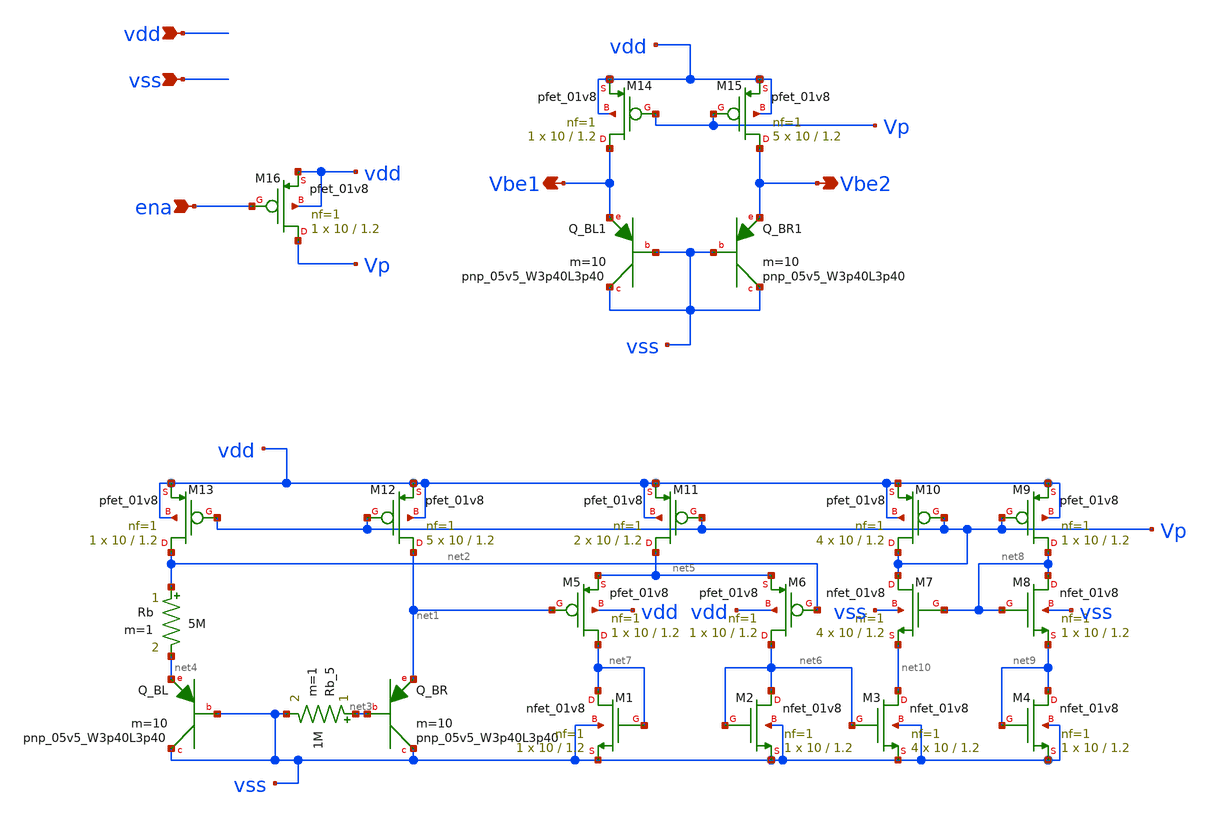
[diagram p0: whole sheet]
** sch_path: xschem/sky130_od_ip__tempsensor.sch
**.subckt sky130_od_ip__tempsensor vdd vss Vbe2 Vbe1 ena
*.ipin vdd
*.ipin vss
*.opin Vbe2
*.opin Vbe1
*.ipin ena
XM12 net1 Vp vdd vdd sky130_fd_pr__pfet_01v8 L=1.2 W=10 nf=1 ad='int((nf+1)/2) * W/nf * 0.29' as='int((nf+2)/2) * W/nf * 0.29'
+ pd='2*int((nf+1)/2) * (W/nf + 0.29)' ps='2*int((nf+2)/2) * (W/nf + 0.29)' nrd='0.29 / W' nrs='0.29 / W'
+ sa=0 sb=0 sd=0 mult=5 m=5
XM13 net2 Vp vdd vdd sky130_fd_pr__pfet_01v8 L=1.2 W=10 nf=1 ad='int((nf+1)/2) * W/nf * 0.29' as='int((nf+2)/2) * W/nf * 0.29'
+ pd='2*int((nf+1)/2) * (W/nf + 0.29)' ps='2*int((nf+2)/2) * (W/nf + 0.29)' nrd='0.29 / W' nrs='0.29 / W'
+ sa=0 sb=0 sd=0 mult=1 m=1
XQ_BR vss net3 net1 sky130_fd_pr__pnp_05v5_W3p40L3p40 m=10
XQ_BL vss vss net4 sky130_fd_pr__pnp_05v5_W3p40L3p40 m=10
Rb net2 net4 5M m=1
Rb_5 net3 vss 1M m=1
XM11 net5 Vp vdd vdd sky130_fd_pr__pfet_01v8 L=1.2 W=10 nf=1 ad='int((nf+1)/2) * W/nf * 0.29' as='int((nf+2)/2) * W/nf * 0.29'
+ pd='2*int((nf+1)/2) * (W/nf + 0.29)' ps='2*int((nf+2)/2) * (W/nf + 0.29)' nrd='0.29 / W' nrs='0.29 / W'
+ sa=0 sb=0 sd=0 mult=2 m=2
XM6 net6 net2 net5 vdd sky130_fd_pr__pfet_01v8 L=1.2 W=10 nf=1 ad='int((nf+1)/2) * W/nf * 0.29' as='int((nf+2)/2) * W/nf * 0.29'
+ pd='2*int((nf+1)/2) * (W/nf + 0.29)' ps='2*int((nf+2)/2) * (W/nf + 0.29)' nrd='0.29 / W' nrs='0.29 / W'
+ sa=0 sb=0 sd=0 mult=1 m=1
XM5 net7 net1 net5 vdd sky130_fd_pr__pfet_01v8 L=1.2 W=10 nf=1 ad='int((nf+1)/2) * W/nf * 0.29' as='int((nf+2)/2) * W/nf * 0.29'
+ pd='2*int((nf+1)/2) * (W/nf + 0.29)' ps='2*int((nf+2)/2) * (W/nf + 0.29)' nrd='0.29 / W' nrs='0.29 / W'
+ sa=0 sb=0 sd=0 mult=1 m=1
XM2 net6 net6 vss vss sky130_fd_pr__nfet_01v8 L=1.2 W=10 nf=1 ad='int((nf+1)/2) * W/nf * 0.29' as='int((nf+2)/2) * W/nf * 0.29'
+ pd='2*int((nf+1)/2) * (W/nf + 0.29)' ps='2*int((nf+2)/2) * (W/nf + 0.29)' nrd='0.29 / W' nrs='0.29 / W'
+ sa=0 sb=0 sd=0 mult=1 m=1
XM1 net7 net7 vss vss sky130_fd_pr__nfet_01v8 L=1.2 W=10 nf=1 ad='int((nf+1)/2) * W/nf * 0.29' as='int((nf+2)/2) * W/nf * 0.29'
+ pd='2*int((nf+1)/2) * (W/nf + 0.29)' ps='2*int((nf+2)/2) * (W/nf + 0.29)' nrd='0.29 / W' nrs='0.29 / W'
+ sa=0 sb=0 sd=0 mult=1 m=1
XM9 net8 Vp vdd vdd sky130_fd_pr__pfet_01v8 L=1.2 W=10 nf=1 ad='int((nf+1)/2) * W/nf * 0.29' as='int((nf+2)/2) * W/nf * 0.29'
+ pd='2*int((nf+1)/2) * (W/nf + 0.29)' ps='2*int((nf+2)/2) * (W/nf + 0.29)' nrd='0.29 / W' nrs='0.29 / W'
+ sa=0 sb=0 sd=0 mult=1 m=1
XM10 Vp Vp vdd vdd sky130_fd_pr__pfet_01v8 L=1.2 W=10 nf=1 ad='int((nf+1)/2) * W/nf * 0.29' as='int((nf+2)/2) * W/nf * 0.29'
+ pd='2*int((nf+1)/2) * (W/nf + 0.29)' ps='2*int((nf+2)/2) * (W/nf + 0.29)' nrd='0.29 / W' nrs='0.29 / W'
+ sa=0 sb=0 sd=0 mult=4 m=4
XM7 Vp net8 net10 vss sky130_fd_pr__nfet_01v8 L=1.2 W=10 nf=1 ad='int((nf+1)/2) * W/nf * 0.29' as='int((nf+2)/2) * W/nf * 0.29'
+ pd='2*int((nf+1)/2) * (W/nf + 0.29)' ps='2*int((nf+2)/2) * (W/nf + 0.29)' nrd='0.29 / W' nrs='0.29 / W'
+ sa=0 sb=0 sd=0 mult=4 m=4
XM8 net8 net8 net9 vss sky130_fd_pr__nfet_01v8 L=1.2 W=10 nf=1 ad='int((nf+1)/2) * W/nf * 0.29' as='int((nf+2)/2) * W/nf * 0.29'
+ pd='2*int((nf+1)/2) * (W/nf + 0.29)' ps='2*int((nf+2)/2) * (W/nf + 0.29)' nrd='0.29 / W' nrs='0.29 / W'
+ sa=0 sb=0 sd=0 mult=1 m=1
XM3 net10 net6 vss vss sky130_fd_pr__nfet_01v8 L=1.2 W=10 nf=1 ad='int((nf+1)/2) * W/nf * 0.29' as='int((nf+2)/2) * W/nf * 0.29'
+ pd='2*int((nf+1)/2) * (W/nf + 0.29)' ps='2*int((nf+2)/2) * (W/nf + 0.29)' nrd='0.29 / W' nrs='0.29 / W'
+ sa=0 sb=0 sd=0 mult=4 m=4
XM4 net9 net9 vss vss sky130_fd_pr__nfet_01v8 L=1.2 W=10 nf=1 ad='int((nf+1)/2) * W/nf * 0.29' as='int((nf+2)/2) * W/nf * 0.29'
+ pd='2*int((nf+1)/2) * (W/nf + 0.29)' ps='2*int((nf+2)/2) * (W/nf + 0.29)' nrd='0.29 / W' nrs='0.29 / W'
+ sa=0 sb=0 sd=0 mult=1 m=1
XQ_BL1 vss vss Vbe1 sky130_fd_pr__pnp_05v5_W3p40L3p40 m=10
XQ_BR1 vss vss Vbe2 sky130_fd_pr__pnp_05v5_W3p40L3p40 m=10
XM14 Vbe1 Vp vdd vdd sky130_fd_pr__pfet_01v8 L=1.2 W=10 nf=1 ad='int((nf+1)/2) * W/nf * 0.29' as='int((nf+2)/2) * W/nf * 0.29'
+ pd='2*int((nf+1)/2) * (W/nf + 0.29)' ps='2*int((nf+2)/2) * (W/nf + 0.29)' nrd='0.29 / W' nrs='0.29 / W'
+ sa=0 sb=0 sd=0 mult=1 m=1
XM15 Vbe2 Vp vdd vdd sky130_fd_pr__pfet_01v8 L=1.2 W=10 nf=1 ad='int((nf+1)/2) * W/nf * 0.29' as='int((nf+2)/2) * W/nf * 0.29'
+ pd='2*int((nf+1)/2) * (W/nf + 0.29)' ps='2*int((nf+2)/2) * (W/nf + 0.29)' nrd='0.29 / W' nrs='0.29 / W'
+ sa=0 sb=0 sd=0 mult=5 m=5
XM16 Vp ena vdd vdd sky130_fd_pr__pfet_01v8 L=1.2 W=10 nf=1 ad='int((nf+1)/2) * W/nf * 0.29' as='int((nf+2)/2) * W/nf * 0.29'
+ pd='2*int((nf+1)/2) * (W/nf + 0.29)' ps='2*int((nf+2)/2) * (W/nf + 0.29)' nrd='0.29 / W' nrs='0.29 / W'
+ sa=0 sb=0 sd=0 mult=1 m=1
**.ends
.end
